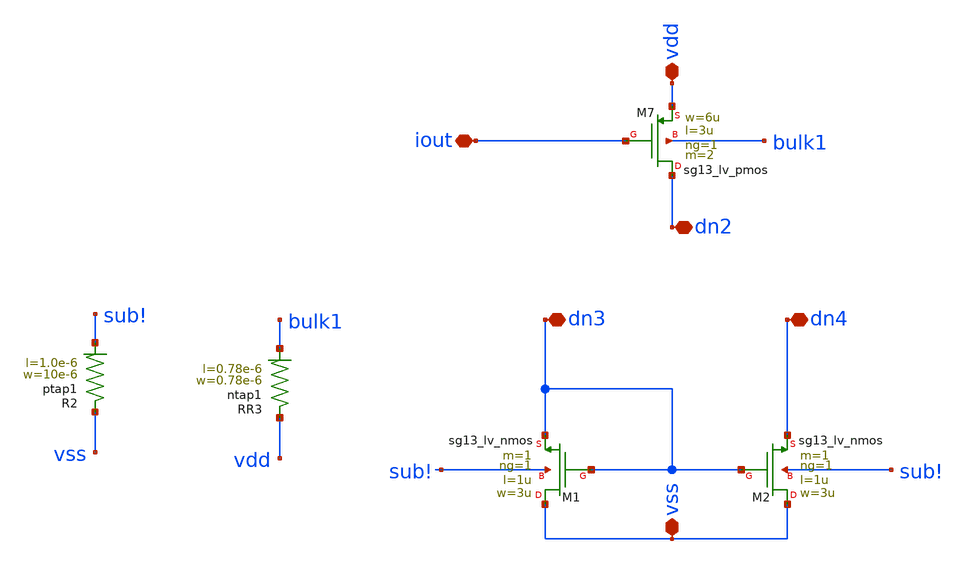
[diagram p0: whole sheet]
** sch_path: dependencies/pmu_ip/dependencies/OTA/OTA-main/schematic/xschem/input_stage.sch
**.subckt input_stage vss vdd dn4 dn3 dn2 iout
*.iopin vss
*.iopin vdd
*.iopin dn4
*.iopin dn3
*.iopin dn2
*.iopin iout
XM7 dn2 iout vdd bulk1 sg13_lv_pmos w=6u l=3u ng=1 m=2 mm_ok=1
XR2 vss sub! ptap1 R=30.62 w=10e-6 l=1.0e-6
XR3 vdd bulk1 ntap1 R=262.8 w=0.78e-6 l=0.78e-6
XM1 vss dn3 dn3 sub! sg13_lv_nmos w=3u l=1u ng=1 m=1 mm_ok=1
XM2 vss dn3 dn4 sub! sg13_lv_nmos w=3u l=1u ng=1 m=1 mm_ok=1
**.ends
.end
